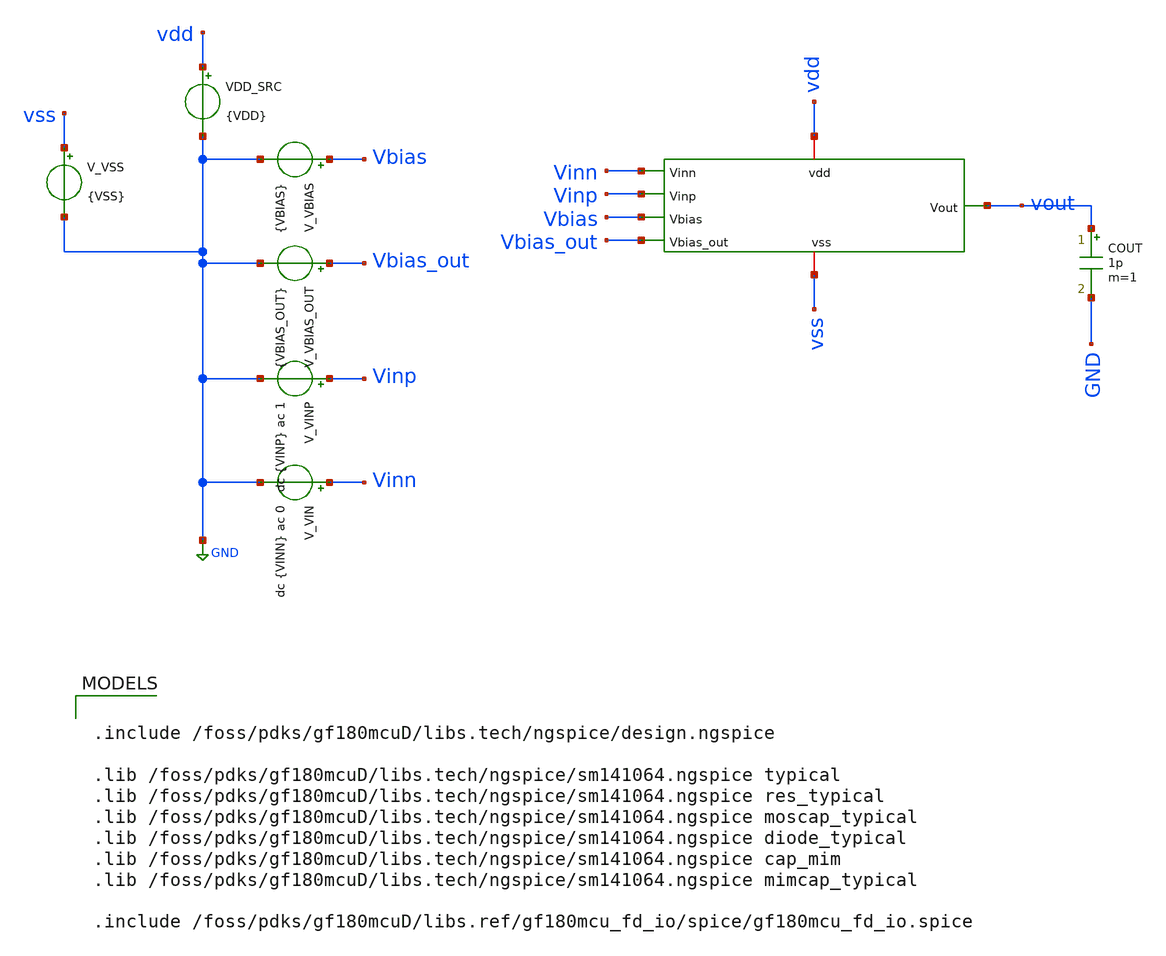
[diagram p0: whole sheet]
** sch_path: circuit_files/sar_adc_test/tb/op-amp_tb.sch
**.subckt op-amp_tb
V_VIN Vinn GND dc {VINN} ac 0
VDD_SRC vdd GND {VDD}
V_VINP Vinp GND dc {VINP} ac 1
V_VBIAS Vbias GND {VBIAS}
V_VSS vss GND {VSS}
V_VBIAS_OUT Vbias_out GND {VBIAS_OUT}
x1 vout Vinn vdd Vinp Vbias vss Vbias_out op-amp
COUT vout GND 1p m=1
**** begin user architecture code

.include /foss/pdks/gf180mcuD/libs.tech/ngspice/design.ngspice

.lib /foss/pdks/gf180mcuD/libs.tech/ngspice/sm141064.ngspice typical
.lib /foss/pdks/gf180mcuD/libs.tech/ngspice/sm141064.ngspice res_typical
.lib /foss/pdks/gf180mcuD/libs.tech/ngspice/sm141064.ngspice moscap_typical
.lib /foss/pdks/gf180mcuD/libs.tech/ngspice/sm141064.ngspice diode_typical
.lib /foss/pdks/gf180mcuD/libs.tech/ngspice/sm141064.ngspice cap_mim
.lib /foss/pdks/gf180mcuD/libs.tech/ngspice/sm141064.ngspice mimcap_typical

.include /foss/pdks/gf180mcuD/libs.ref/gf180mcu_fd_io/spice/gf180mcu_fd_io.spice




.param VDD=3.3
.param VSS=0
.param VCM=1.65
.param VINP={VCM}
.param VINN={VCM}
.param VBIAS=0.70
.param VBIAS_OUT=0.6638

.options savecurrents
.options reltol=1e-4 abstol=1e-12 vntol=1e-6

.control
set filetype=ascii
shell rm -f opamp_final_results.txt opamp_ac.txt

op

echo ============================================= > opamp_final_results.txt
echo GF180MCU two-stage op-amp symbol testbench results >> opamp_final_results.txt
echo ============================================= >> opamp_final_results.txt

echo ---- DC operating point ---- >> opamp_final_results.txt

let idd = -i(VDD_SRC)
let iss = i(V_VSS)
let pdc = v(vdd)*idd

echo Vinp     = $&v(Vinp)      V >> opamp_final_results.txt
echo Vinn     = $&v(Vinn)      V >> opamp_final_results.txt
echo x1.net1  = $&v(x1.net1)   V >> opamp_final_results.txt
echo x1.net2  = $&v(x1.net2)   V >> opamp_final_results.txt
echo x1.Vx    = $&v(x1.Vx)     V >> opamp_final_results.txt
echo Vout     = $&v(vout)      V >> opamp_final_results.txt
echo IDD      = $&idd          A >> opamp_final_results.txt
echo ISS      = $&iss          A >> opamp_final_results.txt
echo PDC      = $&pdc          W >> opamp_final_results.txt
echo . >> opamp_final_results.txt

echo ---- MOS operating point data ---- >> opamp_final_results.txt
show m.x1.xm1.m0 >> opamp_final_results.txt
show m.x1.xm2.m0 >> opamp_final_results.txt
show m.x1.xm3.m0 >> opamp_final_results.txt
show m.x1.xm4.m0 >> opamp_final_results.txt
show m.x1.xm5.m0 >> opamp_final_results.txt
show m.x1.xm7.m0 >> opamp_final_results.txt
show m.x1.xm8.m0 >> opamp_final_results.txt

ac dec 100 1 1e9

meas ac av_1hz_db FIND vdb(vout) AT=1
meas ac ugf WHEN vdb(vout)=0 FALL=1
meas ac phase_rad FIND vp(vout) WHEN vdb(vout)=0 FALL=1

let phase_deg = phase_rad*180/pi
let phase_margin = 180 + phase_deg

echo . >> opamp_final_results.txt
echo ---- AC open-loop results ---- >> opamp_final_results.txt
echo DC_gain_approx_1Hz = $&av_1hz_db dB >> opamp_final_results.txt
echo UGF                = $&ugf Hz >> opamp_final_results.txt
echo Phase_at_UGF       = $&phase_deg deg >> opamp_final_results.txt
echo Phase_margin       = $&phase_margin deg >> opamp_final_results.txt
echo . >> opamp_final_results.txt

wrdata opamp_ac.txt frequency vdb(vout) vp(vout)

.endc


**** end user architecture code
**.ends
.GLOBAL GND
.end
